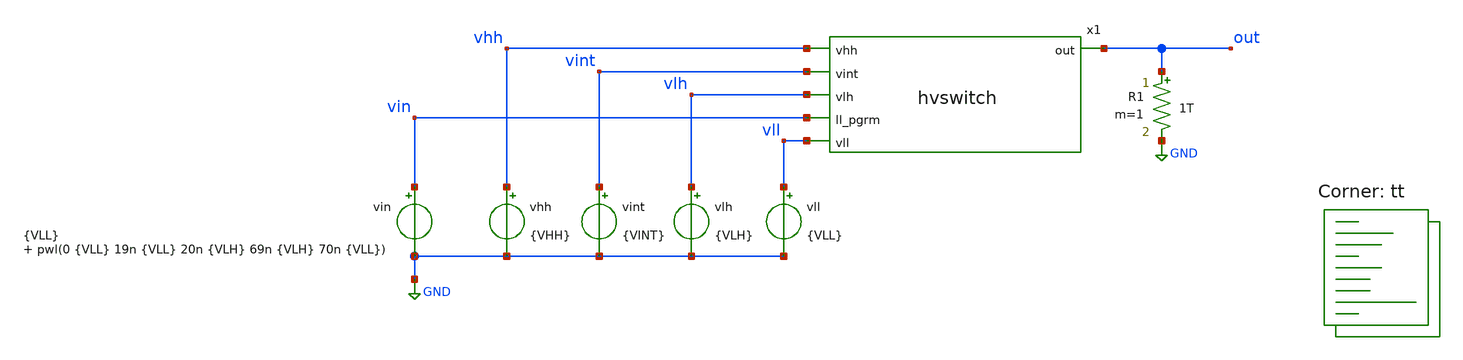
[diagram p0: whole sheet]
** sch_path: test-hvswitch.sch
**.subckt test-hvswitch
x1 vhh out vint vlh vin vll hvswitch
vhh vhh GND {VHH}
vint vint GND {VINT}
vlh vlh GND {VLH}
vll vll GND {VLL}
vin vin GND {VLL} pwl(0 {VLL} 19n {VLL} 20n {VLH} 69n {VLH} 70n {VLL})
R1 out GND 1T m=1
**** begin user architecture code
.lib $::SKYWATER_MODELS/sky130.lib.spice tt



.param VLL=0
.param VLH=1.8
.param VHH=6
.param VINT={(VHH+VLL)/2}
.option savecurrents
.control
  save all
  op
  remzerovec
  write test-hvswitch.raw
  set appendwrite
  tran 10p 100n
  remzerovec
  write test-hvswitch.raw
.endc



**** end user architecture code
**.ends

* expanding   symbol:  hvswitch.sym # of pins=6
** sym_path: hvswitch.sym
** sch_path: hvswitch.sch
.subckt hvswitch vhh out vint vlh ll_pgrm vll
*.ipin ll_pgrm
*.ipin vhh
*.ipin vll
*.opin out
*.ipin vlh
*.ipin vint
XMN1 n1 ll_pgrm vll vll sky130_fd_pr__nfet_g5v0d10v5 L=0.5 W=1 nf=1 ad='int((nf+1)/2) * W/nf * 0.29'
+ as='int((nf+2)/2) * W/nf * 0.29' pd='2*int((nf+1)/2) * (W/nf + 0.29)' ps='2*int((nf+2)/2) * (W/nf + 0.29)'
+ nrd='0.29 / W' nrs='0.29 / W' sa=0 sb=0 sd=0 mult=1 m=1
XMN2 A vint n1 vll sky130_fd_pr__nfet_g5v0d10v5 L=0.5 W=1 nf=1 ad='int((nf+1)/2) * W/nf * 0.29' as='int((nf+2)/2) * W/nf * 0.29'
+ pd='2*int((nf+1)/2) * (W/nf + 0.29)' ps='2*int((nf+2)/2) * (W/nf + 0.29)' nrd='0.29 / W' nrs='0.29 / W'
+ sa=0 sb=0 sd=0 mult=1 m=1
XMN3 n2 ll_pgrm_b vll vll sky130_fd_pr__nfet_g5v0d10v5 L=0.5 W=1 nf=1 ad='int((nf+1)/2) * W/nf * 0.29'
+ as='int((nf+2)/2) * W/nf * 0.29' pd='2*int((nf+1)/2) * (W/nf + 0.29)' ps='2*int((nf+2)/2) * (W/nf + 0.29)'
+ nrd='0.29 / W' nrs='0.29 / W' sa=0 sb=0 sd=0 mult=1 m=1
XMN4 B vint n2 vll sky130_fd_pr__nfet_g5v0d10v5 L=0.5 W=1 nf=1 ad='int((nf+1)/2) * W/nf * 0.29' as='int((nf+2)/2) * W/nf * 0.29'
+ pd='2*int((nf+1)/2) * (W/nf + 0.29)' ps='2*int((nf+2)/2) * (W/nf + 0.29)' nrd='0.29 / W' nrs='0.29 / W'
+ sa=0 sb=0 sd=0 mult=1 m=1
XMP1 p1 C vhh vhh sky130_fd_pr__pfet_g5v0d10v5 L=0.5 W=1 nf=1 ad='int((nf+1)/2) * W/nf * 0.29' as='int((nf+2)/2) * W/nf * 0.29'
+ pd='2*int((nf+1)/2) * (W/nf + 0.29)' ps='2*int((nf+2)/2) * (W/nf + 0.29)' nrd='0.29 / W' nrs='0.29 / W'
+ sa=0 sb=0 sd=0 mult=1 m=1
XMP2 A vint p1 vhh sky130_fd_pr__pfet_g5v0d10v5 L=0.5 W=1 nf=1 ad='int((nf+1)/2) * W/nf * 0.29' as='int((nf+2)/2) * W/nf * 0.29'
+ pd='2*int((nf+1)/2) * (W/nf + 0.29)' ps='2*int((nf+2)/2) * (W/nf + 0.29)' nrd='0.29 / W' nrs='0.29 / W'
+ sa=0 sb=0 sd=0 mult=1 m=1
XMP3 p2 out vhh vhh sky130_fd_pr__pfet_g5v0d10v5 L=0.5 W=1 nf=1 ad='int((nf+1)/2) * W/nf * 0.29' as='int((nf+2)/2) * W/nf * 0.29'
+ pd='2*int((nf+1)/2) * (W/nf + 0.29)' ps='2*int((nf+2)/2) * (W/nf + 0.29)' nrd='0.29 / W' nrs='0.29 / W'
+ sa=0 sb=0 sd=0 mult=1 m=1
XMP4 B vint p2 vhh sky130_fd_pr__pfet_g5v0d10v5 L=0.5 W=1 nf=1 ad='int((nf+1)/2) * W/nf * 0.29' as='int((nf+2)/2) * W/nf * 0.29'
+ pd='2*int((nf+1)/2) * (W/nf + 0.29)' ps='2*int((nf+2)/2) * (W/nf + 0.29)' nrd='0.29 / W' nrs='0.29 / W'
+ sa=0 sb=0 sd=0 mult=1 m=1
XMF1 vint A out vhh sky130_fd_pr__pfet_g5v0d10v5 L=0.5 W=1 nf=1 ad='int((nf+1)/2) * W/nf * 0.29' as='int((nf+2)/2) * W/nf * 0.29'
+ pd='2*int((nf+1)/2) * (W/nf + 0.29)' ps='2*int((nf+2)/2) * (W/nf + 0.29)' nrd='0.29 / W' nrs='0.29 / W'
+ sa=0 sb=0 sd=0 mult=1 m=1
XMF2 A vint out vhh sky130_fd_pr__pfet_g5v0d10v5 L=0.5 W=1 nf=1 ad='int((nf+1)/2) * W/nf * 0.29' as='int((nf+2)/2) * W/nf * 0.29'
+ pd='2*int((nf+1)/2) * (W/nf + 0.29)' ps='2*int((nf+2)/2) * (W/nf + 0.29)' nrd='0.29 / W' nrs='0.29 / W'
+ sa=0 sb=0 sd=0 mult=1 m=1
XMF3 vint B C vhh sky130_fd_pr__pfet_g5v0d10v5 L=0.5 W=1 nf=1 ad='int((nf+1)/2) * W/nf * 0.29' as='int((nf+2)/2) * W/nf * 0.29'
+ pd='2*int((nf+1)/2) * (W/nf + 0.29)' ps='2*int((nf+2)/2) * (W/nf + 0.29)' nrd='0.29 / W' nrs='0.29 / W'
+ sa=0 sb=0 sd=0 mult=1 m=1
XMF4 B vint C vhh sky130_fd_pr__pfet_g5v0d10v5 L=0.5 W=1 nf=1 ad='int((nf+1)/2) * W/nf * 0.29' as='int((nf+2)/2) * W/nf * 0.29'
+ pd='2*int((nf+1)/2) * (W/nf + 0.29)' ps='2*int((nf+2)/2) * (W/nf + 0.29)' nrd='0.29 / W' nrs='0.29 / W'
+ sa=0 sb=0 sd=0 mult=1 m=1
XMP5 ll_pgrm_b ll_pgrm vlh vlh sky130_fd_pr__pfet_g5v0d10v5 L=0.5 W=1 nf=1 ad='int((nf+1)/2) * W/nf * 0.29'
+ as='int((nf+2)/2) * W/nf * 0.29' pd='2*int((nf+1)/2) * (W/nf + 0.29)' ps='2*int((nf+2)/2) * (W/nf + 0.29)'
+ nrd='0.29 / W' nrs='0.29 / W' sa=0 sb=0 sd=0 mult=1 m=1
XMN5 ll_pgrm_b ll_pgrm vll vll sky130_fd_pr__nfet_g5v0d10v5 L=0.5 W=1 nf=1 ad='int((nf+1)/2) * W/nf * 0.29'
+ as='int((nf+2)/2) * W/nf * 0.29' pd='2*int((nf+1)/2) * (W/nf + 0.29)' ps='2*int((nf+2)/2) * (W/nf + 0.29)'
+ nrd='0.29 / W' nrs='0.29 / W' sa=0 sb=0 sd=0 mult=1 m=1
.save v(a)
.save v(b)
.save v(c)
.save v(out)
.save v(p1)
.save v(p2)
.save v(n1)
.save v(n2)
.save v(vint)
.save v(ll_pgrm)
.save v(ll_pgrm_b)
.ends

.GLOBAL GND
.end
